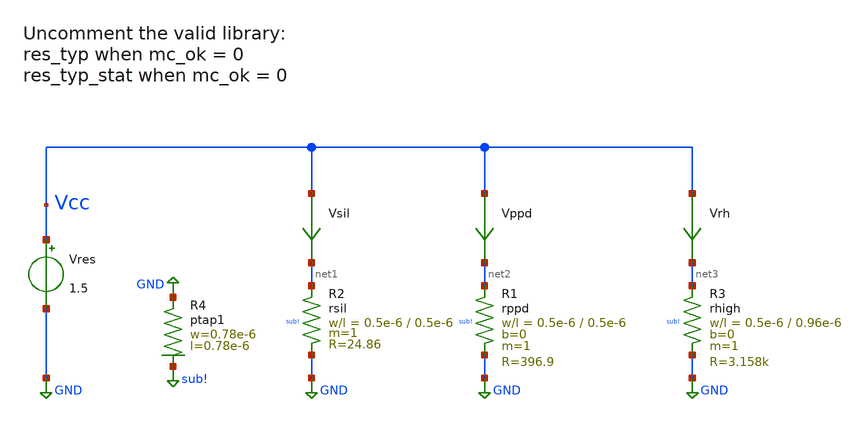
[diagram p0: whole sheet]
** sch_path: ihp-sg13g2/xschem_libs/sg13g2_tests_ase/mc_res_op/schematic/mc_res_op.sch
* Copyright 2023 IHP PDK Authors
**.subckt mc_res_op
Vres Vcc GND 1.5
Vsil Vcc net1 0
.save i(vsil)
Vppd Vcc net2 0
.save i(vppd)
Vrh Vcc net3 0
.save i(vrh)
XR1 net2 GND sub! rppd w=0.5e-6 l=0.5e-6 m=1 b=0 mm_ok=1
XR2 net1 GND sub! rsil w=0.5e-6 l=0.5e-6 m=1 mm_ok=1
XR3 net3 GND sub! rhigh w=0.5e-6 l=0.96e-6 m=1 b=0 mm_ok=1
XR4 GND sub! ptap1 R=262.8 w=0.78e-6 l=0.78e-6
**.ends
.GLOBAL GND
.GLOBAL sub!
.end
